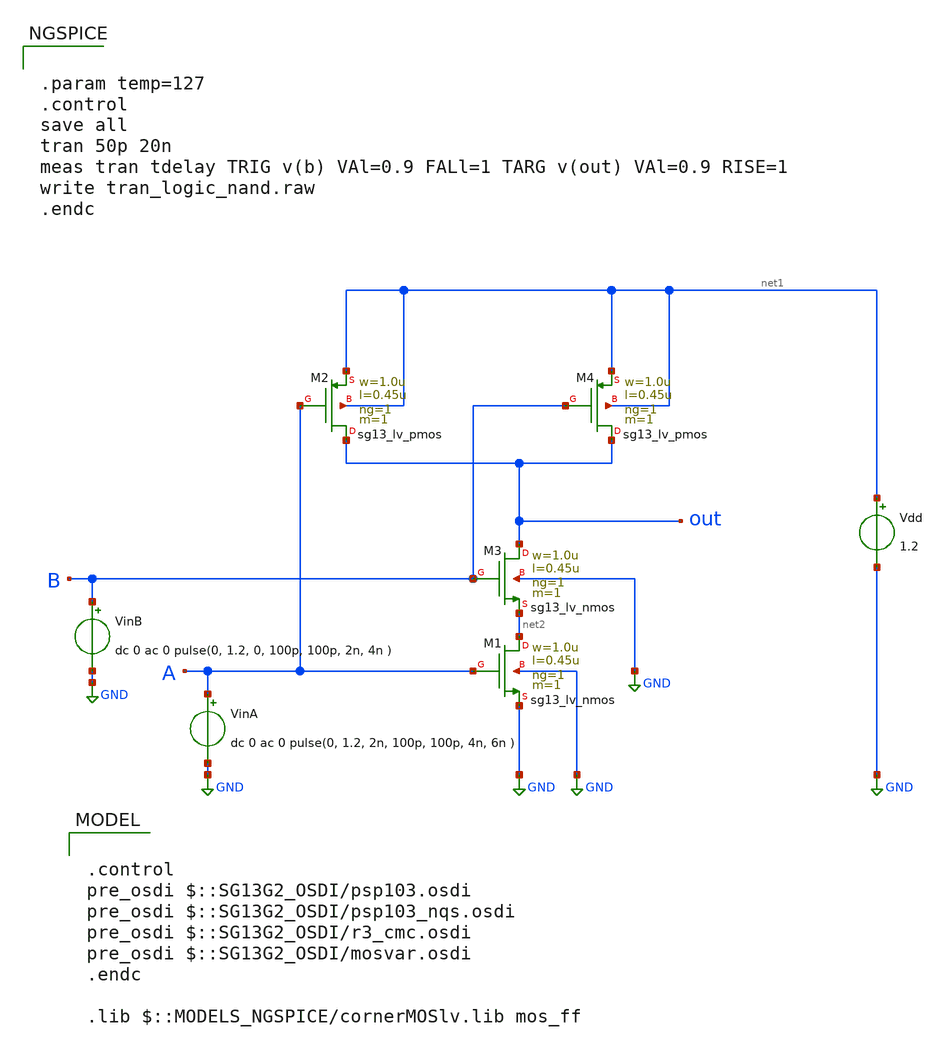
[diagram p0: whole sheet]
** sch_path: ihp-sg13g2/xschem_libs/sg13g2_tests/tran_logic_nand/schematic/tran_logic_nand.sch
* Copyright 2023 IHP PDK Authors
**.subckt tran_logic_nand
VinA A GND dc 0 ac 0 pulse(0, 1.2, 2n, 100p, 100p, 4n, 6n )
Vdd net1 GND 1.2
VinB B GND dc 0 ac 0 pulse(0, 1.2, 0, 100p, 100p, 2n, 4n )
XM1 net2 A GND GND sg13_lv_nmos w=1.0u l=0.45u ng=1 m=1 mm_ok=1
XM3 out B net2 GND sg13_lv_nmos w=1.0u l=0.45u ng=1 m=1 mm_ok=1
XM2 out A net1 net1 sg13_lv_pmos w=1.0u l=0.45u ng=1 m=1 mm_ok=1
XM4 out B net1 net1 sg13_lv_pmos w=1.0u l=0.45u ng=1 m=1 mm_ok=1
**** begin user architecture code

.control
pre_osdi $::SG13G2_OSDI/psp103.osdi
pre_osdi $::SG13G2_OSDI/psp103_nqs.osdi
pre_osdi $::SG13G2_OSDI/r3_cmc.osdi
pre_osdi $::SG13G2_OSDI/mosvar.osdi
.endc

.lib $::MODELS_NGSPICE/cornerMOSlv.lib mos_ff



.param temp=127
.control
save all
tran 50p 20n
meas tran tdelay TRIG v(b) VAl=0.9 FALl=1 TARG v(out) VAl=0.9 RISE=1
write tran_logic_nand.raw
.endc


**** end user architecture code
**.ends
.GLOBAL GND
.end
